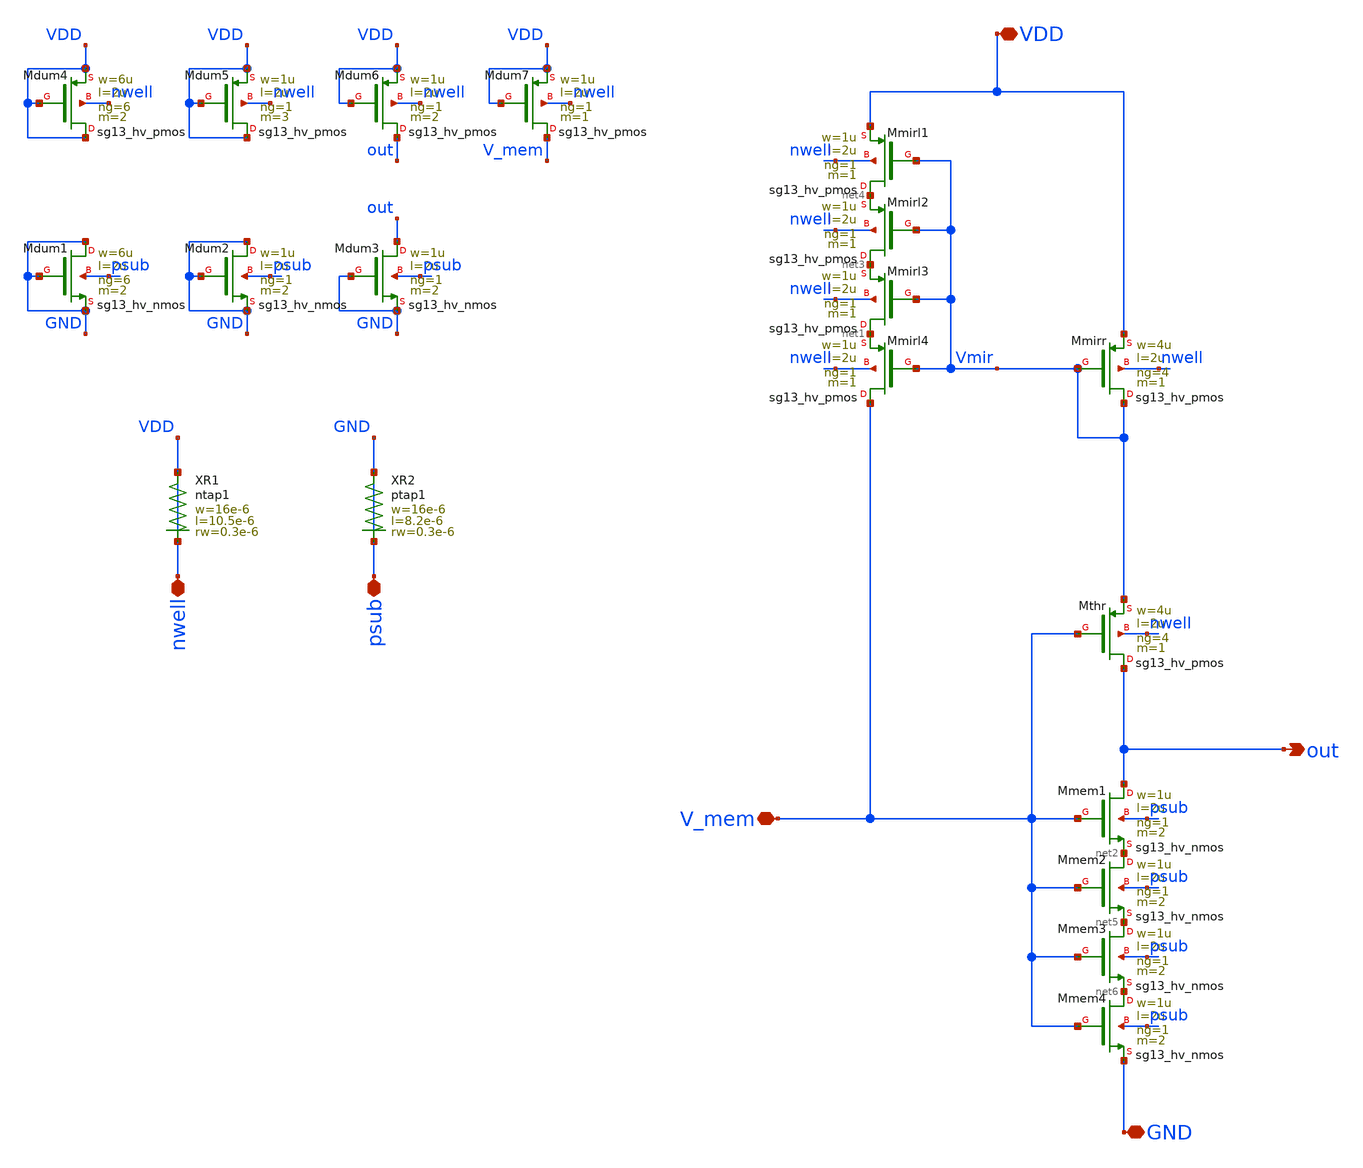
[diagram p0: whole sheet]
** sch_path: xschem/FB_system_BK.sch
**.subckt FB_system_BK out V_mem VDD GND nwell psub
*.opin out
*.iopin V_mem
*.iopin VDD
*.iopin GND
*.iopin nwell
*.iopin psub
XMmirr Vmir Vmir VDD nwell sg13_hv_pmos w=4u l=2u ng=4 m=1 mm_ok=1
XMmirl4 V_mem Vmir net1 nwell sg13_hv_pmos w=1u l=2u ng=1 m=1 mm_ok=1
XMthr out V_mem Vmir nwell sg13_hv_pmos w=4u l=2u ng=4 m=1 mm_ok=1
XMmem1 out V_mem net2 psub sg13_hv_nmos w=1u l=2u ng=1 m=2 mm_ok=1
XMmirl3 net1 Vmir net3 nwell sg13_hv_pmos w=1u l=2u ng=1 m=1 mm_ok=1
XMmirl2 net3 Vmir net4 nwell sg13_hv_pmos w=1u l=2u ng=1 m=1 mm_ok=1
XMmirl1 net4 Vmir VDD nwell sg13_hv_pmos w=1u l=2u ng=1 m=1 mm_ok=1
XMmem2 net2 V_mem net5 psub sg13_hv_nmos w=1u l=2u ng=1 m=2 mm_ok=1
XMmem3 net5 V_mem net6 psub sg13_hv_nmos w=1u l=2u ng=1 m=2 mm_ok=1
XMmem4 net6 V_mem GND psub sg13_hv_nmos w=1u l=2u ng=1 m=2 mm_ok=1
XMdum1 GND GND GND psub sg13_hv_nmos w=6u l=2u ng=6 m=2 mm_ok=1
XMdum2 GND GND GND psub sg13_hv_nmos w=1u l=2u ng=1 m=2 mm_ok=1
XMdum3 out GND GND psub sg13_hv_nmos w=1u l=2u ng=1 m=2 mm_ok=1
XMdum4 VDD VDD VDD nwell sg13_hv_pmos w=6u l=2u ng=6 m=2 mm_ok=1
XMdum5 VDD VDD VDD nwell sg13_hv_pmos w=1u l=2u ng=1 m=3 mm_ok=1
XMdum6 out VDD VDD nwell sg13_hv_pmos w=1u l=2u ng=1 m=2 mm_ok=1
XMdum7 V_mem VDD VDD nwell sg13_hv_pmos w=1u l=2u ng=1 m=1 mm_ok=1
XR1 VDD VDD ntap1 R=4.4 w=16e-6 l=10.5e-6 rw=0.3e-6
XR2 GND GND ptap1 R=4.829 w=16e-6 l=8.2e-6 rw=0.3e-6
**.ends
.end
